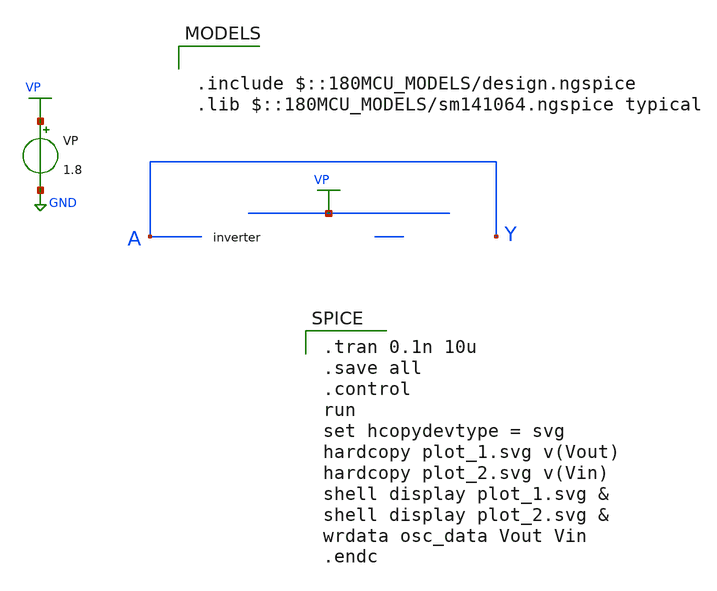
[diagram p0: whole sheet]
** sch_path: TopLevel_oscillator_extracted.sch
**.subckt TopLevel_oscillator_extracted
VP VP GND 1.8
**** begin user architecture code

.include $::180MCU_MODELS/design.ngspice
.lib $::180MCU_MODELS/sm141064.ngspice typical


.tran 0.1n 10u
.save all
.control
run
set hcopydevtype = svg
hardcopy plot_1.svg v(Vout)
hardcopy plot_2.svg v(Vin)
shell display plot_1.svg &
shell display plot_2.svg &
wrdata osc_data Vout Vin
.endc

**** end user architecture code
**.ends
.GLOBAL VP
.GLOBAL GND
.end
